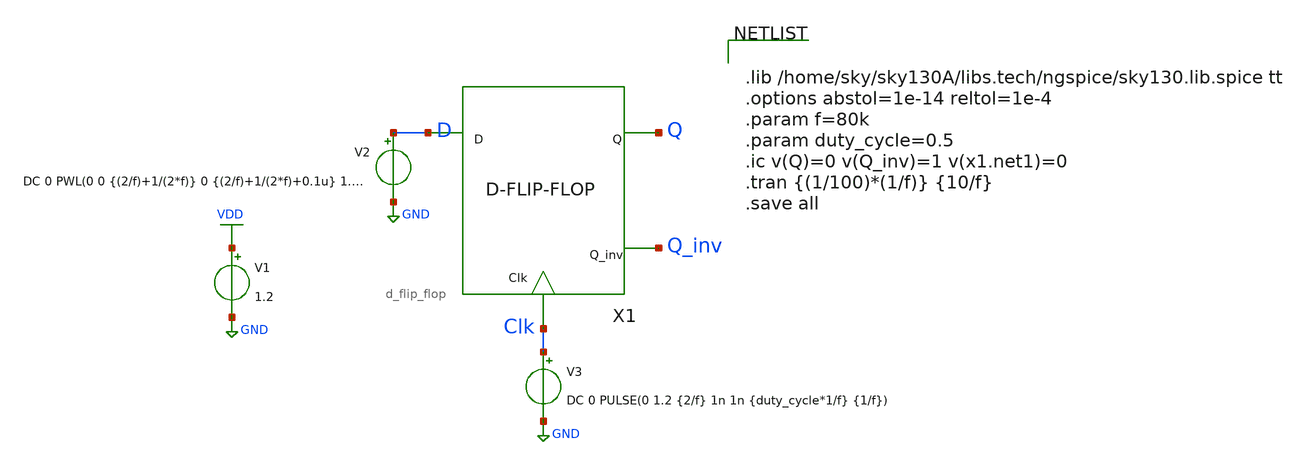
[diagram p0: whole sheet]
** sch_path: xschem/D_flip_flop/d_flip_flop_tb.sch
**.subckt d_flip_flop_tb
V1 VDD GND 1.2
V2 D GND DC 0 PWL(0 0 {(2/f)+1/(2*f)} 0 {(2/f)+1/(2*f)+0.1u} 1.2 {(2/f)+4/(2*f)} 1.2 {(2/f)+4/(2*f)+0.1u}
+ 0)
V3 Clk GND DC 0 PULSE(0 1.2 {2/f} 1n 1n {duty_cycle*1/f} {1/f})
X1 D Q Q_inv Clk d_flip_flop
**** begin user architecture code


.lib /home/sky/sky130A/libs.tech/ngspice/sky130.lib.spice tt
.options abstol=1e-14 reltol=1e-4
.param f=80k
.param duty_cycle=0.5
.ic v(Q)=0 v(Q_inv)=1 v(x1.net1)=0
.tran {(1/100)*(1/f)} {10/f}
.save all


**** end user architecture code
**.ends

* expanding   symbol:  D_flip_flop/d_flip_flop.sym # of pins=4
** sym_path: xschem/D_flip_flop/d_flip_flop.sym
** sch_path: xschem/D_flip_flop/d_flip_flop.sch
.subckt d_flip_flop D Q Q_inv Clk
*.ipin D
*.ipin Clk
*.opin Q_inv
*.opin Q
X1 net1 net2 inv Wpmos=3 Lpmos=0.18 Wnmos=1 Lnmos=0.18
X2 net3 Q inv Wpmos=3 Lpmos=0.18 Wnmos=1 Lnmos=0.18
X3 net2 net4 inv Wpmos=3 Lpmos=0.18 Wnmos=1 Lnmos=0.18
X4 Q Q_inv inv Wpmos=3 Lpmos=0.18 Wnmos=1 Lnmos=0.18
X5 D net1 Clk Clk_inv transmission_gate Wpmos=1 Lpmos=0.18 Wnmos=1 Lnmos=0.18
X6 net1 net4 Clk_inv Clk transmission_gate Wpmos=1 Lpmos=0.18 Wnmos=1 Lnmos=0.18
X7 net3 Q_inv Clk Clk_inv transmission_gate Wpmos=1 Lpmos=0.18 Wnmos=1 Lnmos=0.18
X8 net2 net3 Clk_inv Clk transmission_gate Wpmos=1 Lpmos=0.18 Wnmos=1 Lnmos=0.18
X9 Clk Clk_inv inv Wpmos=3 Lpmos=0.18 Wnmos=1 Lnmos=0.18
.ends


* expanding   symbol:  inv/inv.sym # of pins=2
** sym_path: xschem/inv/inv.sym
** sch_path: xschem/inv/inv.sch
.subckt inv in out  Wpmos=3 Lpmos=0.18 Wnmos=1 Lnmos=0.18
*.ipin in
*.iopin out
XM1 out in GND GND sky130_fd_pr__nfet_01v8 L=Lnmos W=Wnmos nf=1 ad='int((nf+1)/2) * W/nf * 0.29' as='int((nf+2)/2) * W/nf * 0.29'
+ pd='2*int((nf+1)/2) * (W/nf + 0.29)' ps='2*int((nf+2)/2) * (W/nf + 0.29)' nrd='0.29 / W' nrs='0.29 / W'
+ sa=0 sb=0 sd=0 mult=1 m=1
XM2 out in VDD VDD sky130_fd_pr__pfet_01v8 L=Lpmos W=Wpmos nf=1 ad='int((nf+1)/2) * W/nf * 0.29' as='int((nf+2)/2) * W/nf * 0.29'
+ pd='2*int((nf+1)/2) * (W/nf + 0.29)' ps='2*int((nf+2)/2) * (W/nf + 0.29)' nrd='0.29 / W' nrs='0.29 / W'
+ sa=0 sb=0 sd=0 mult=1 m=1
.ends


* expanding   symbol:  transmission_gate/transmission_gate.sym # of pins=4
** sym_path: xschem/transmission_gate/transmission_gate.sym
** sch_path: xschem/transmission_gate/transmission_gate.sch
.subckt transmission_gate in out ctrl_ ctrl  Wpmos=1 Lpmos=0.18 Wnmos=1 Lnmos=0.18
*.iopin in
*.iopin out
*.ipin ctrl_
*.ipin ctrl
XM1 in ctrl out GND sky130_fd_pr__nfet_01v8 L=Lnmos W=Wnmos nf=1 ad='int((nf+1)/2) * W/nf * 0.29' as='int((nf+2)/2) * W/nf * 0.29'
+ pd='2*int((nf+1)/2) * (W/nf + 0.29)' ps='2*int((nf+2)/2) * (W/nf + 0.29)' nrd='0.29 / W' nrs='0.29 / W'
+ sa=0 sb=0 sd=0 mult=1 m=1
XM2 out ctrl_ in VDD sky130_fd_pr__pfet_01v8 L=Lpmos W=Wpmos nf=1 ad='int((nf+1)/2) * W/nf * 0.29' as='int((nf+2)/2) * W/nf * 0.29'
+ pd='2*int((nf+1)/2) * (W/nf + 0.29)' ps='2*int((nf+2)/2) * (W/nf + 0.29)' nrd='0.29 / W' nrs='0.29 / W'
+ sa=0 sb=0 sd=0 mult=1 m=1
.ends

.GLOBAL VDD
.GLOBAL GND
.end
